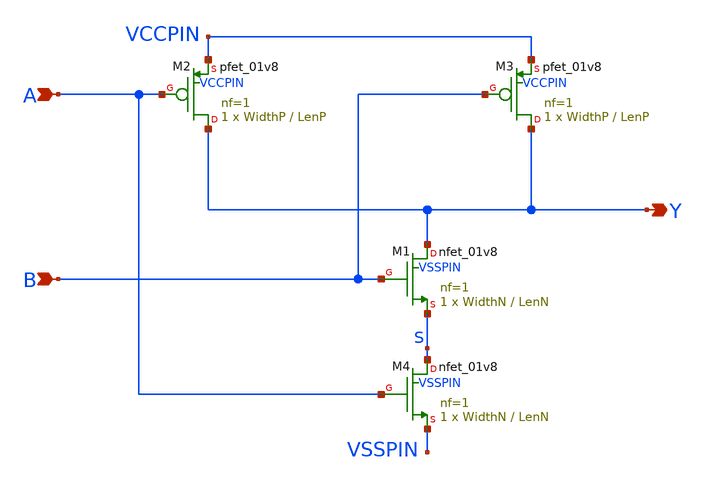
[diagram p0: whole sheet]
** sch_path: sky130_tests/lvnand.sch
* Copyright 2021 Stefan Frederik Schippers
* Licensed under the Apache License, Version 2.0 (the "License");
* you may not use this file except in compliance with the License.
* You may obtain a copy of the License at
* https://www.apache.org/licenses/LICENSE-2.0
* Unless required by applicable law or agreed to in writing, software
* distributed under the License is distributed on an "AS IS" BASIS,
* WITHOUT WARRANTIES OR CONDITIONS OF ANY KIND, either express or implied.
* See the License for the specific language governing permissions and
* limitations under the License.
**.subckt lvnand A B Y
*.ipin A
*.ipin B
*.opin Y
XM1 Y B S VSSPIN sky130_fd_pr__nfet_01v8 L=LenN W=WidthN nf=1 ad='int((1 + 1)/2) * WidthN / 1 * 0.29'
+ as='int((1 + 2)/2) * WidthN / 1 * 0.29' pd='2*int((1 + 1)/2) * (WidthN / 1 + 0.29)' ps='2*int((1 + 2)/2) * (WidthN / 1 + 0.29)'
+ nrd='0.29 / WidthN ' nrs='0.29 / WidthN ' sa=0 sb=0 sd=0 mult=1 m=1
XM2 Y A VCCPIN VCCPIN sky130_fd_pr__pfet_01v8 L=LenP W=WidthP nf=1 ad='int((1 + 1)/2) * WidthP / 1 * 0.29'
+ as='int((1 + 2)/2) * WidthP / 1 * 0.29' pd='2*int((1 + 1)/2) * (WidthP / 1 + 0.29)' ps='2*int((1 + 2)/2) * (WidthP / 1 + 0.29)'
+ nrd='0.29 / WidthP ' nrs='0.29 / WidthP ' sa=0 sb=0 sd=0 mult=1 m=1
XM3 Y B VCCPIN VCCPIN sky130_fd_pr__pfet_01v8 L=LenP W=WidthP nf=1 ad='int((1 + 1)/2) * WidthP / 1 * 0.29'
+ as='int((1 + 2)/2) * WidthP / 1 * 0.29' pd='2*int((1 + 1)/2) * (WidthP / 1 + 0.29)' ps='2*int((1 + 2)/2) * (WidthP / 1 + 0.29)'
+ nrd='0.29 / WidthP ' nrs='0.29 / WidthP ' sa=0 sb=0 sd=0 mult=1 m=1
XM4 S A VSSPIN VSSPIN sky130_fd_pr__nfet_01v8 L=LenN W=WidthN nf=1 ad='int((1 + 1)/2) * WidthN / 1 * 0.29'
+ as='int((1 + 2)/2) * WidthN / 1 * 0.29' pd='2*int((1 + 1)/2) * (WidthN / 1 + 0.29)' ps='2*int((1 + 2)/2) * (WidthN / 1 + 0.29)'
+ nrd='0.29 / WidthN ' nrs='0.29 / WidthN ' sa=0 sb=0 sd=0 mult=1 m=1
**** begin user architecture code

** opencircuitdesign pdks install
.lib $::SKYWATER_MODELS/sky130.lib.spice tt_mm

**** end user architecture code
**.ends
**** begin user architecture code

* .option SCALE=1e-6
.option method=gear seed=12
.param L=0.15
.param W=0.5
vd d 0 0
vg g 0 0
.control
dc vd 0 2 0.01 vg 0 2 0.2
alterparam L=0.18
alterparam W=1
reset
dc vd 0 2 0.01 vg 0 2 0.2
alterparam L=0.3
alterparam W=2
reset
dc vd 0 2 0.01 vg 0 2 0.2
alterparam L=0.5
alterparam W=3
reset
dc vd 0 2 0.01 vg 0 2 0.2
.endc


**** end user architecture code
.end
